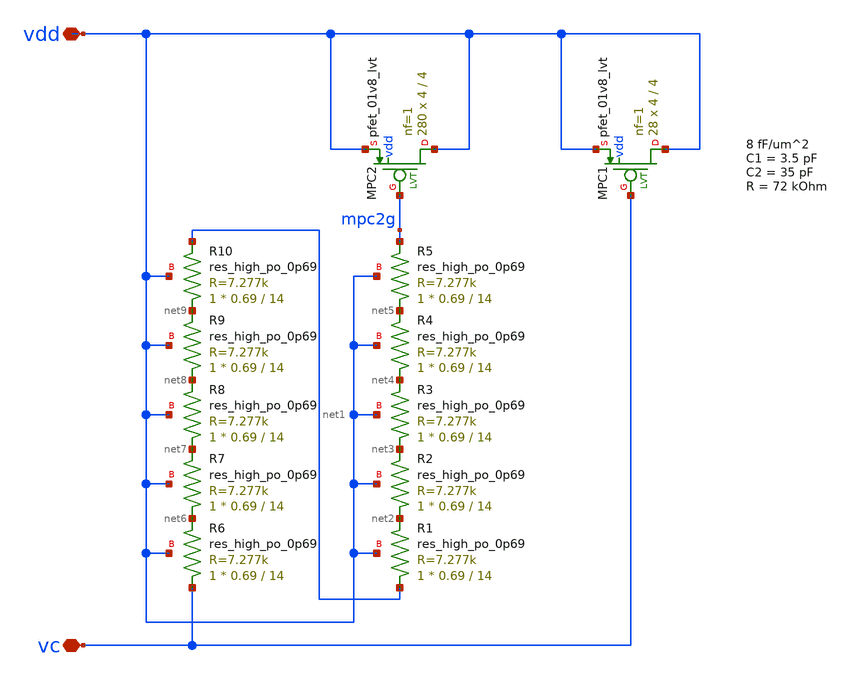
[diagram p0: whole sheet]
** sch_path: xschem/ejf_pll96_lpf.sch
**.subckt ejf_pll96_lpf vc vdd
*.iopin vc
*.iopin vdd
XR1 net1 net2 vdd sky130_fd_pr__res_high_po_0p69 L=14 mult=1 m=1
XR2 net2 net3 vdd sky130_fd_pr__res_high_po_0p69 L=14 mult=1 m=1
XR3 net3 net4 vdd sky130_fd_pr__res_high_po_0p69 L=14 mult=1 m=1
XR4 net4 net5 vdd sky130_fd_pr__res_high_po_0p69 L=14 mult=1 m=1
XR5 net5 mpc2g vdd sky130_fd_pr__res_high_po_0p69 L=14 mult=1 m=1
XR6 vc net6 vdd sky130_fd_pr__res_high_po_0p69 L=14 mult=1 m=1
XR7 net6 net7 vdd sky130_fd_pr__res_high_po_0p69 L=14 mult=1 m=1
XR8 net7 net8 vdd sky130_fd_pr__res_high_po_0p69 L=14 mult=1 m=1
XR9 net8 net9 vdd sky130_fd_pr__res_high_po_0p69 L=14 mult=1 m=1
XR10 net9 net1 vdd sky130_fd_pr__res_high_po_0p69 L=14 mult=1 m=1
XMPC2 vdd mpc2g vdd vdd sky130_fd_pr__pfet_01v8_lvt L=4 W=4 nf=1 ad='int((nf+1)/2) * W/nf * 0.29' as='int((nf+2)/2) * W/nf * 0.29'
+ pd='2*int((nf+1)/2) * (W/nf + 0.29)' ps='2*int((nf+2)/2) * (W/nf + 0.29)' nrd='0.29 / W' nrs='0.29 / W'
+ sa=0 sb=0 sd=0 mult=280 m=280
XMPC1 vdd vc vdd vdd sky130_fd_pr__pfet_01v8_lvt L=4 W=4 nf=1 ad='int((nf+1)/2) * W/nf * 0.29' as='int((nf+2)/2) * W/nf * 0.29'
+ pd='2*int((nf+1)/2) * (W/nf + 0.29)' ps='2*int((nf+2)/2) * (W/nf + 0.29)' nrd='0.29 / W' nrs='0.29 / W'
+ sa=0 sb=0 sd=0 mult=28 m=28
**.ends
.end
